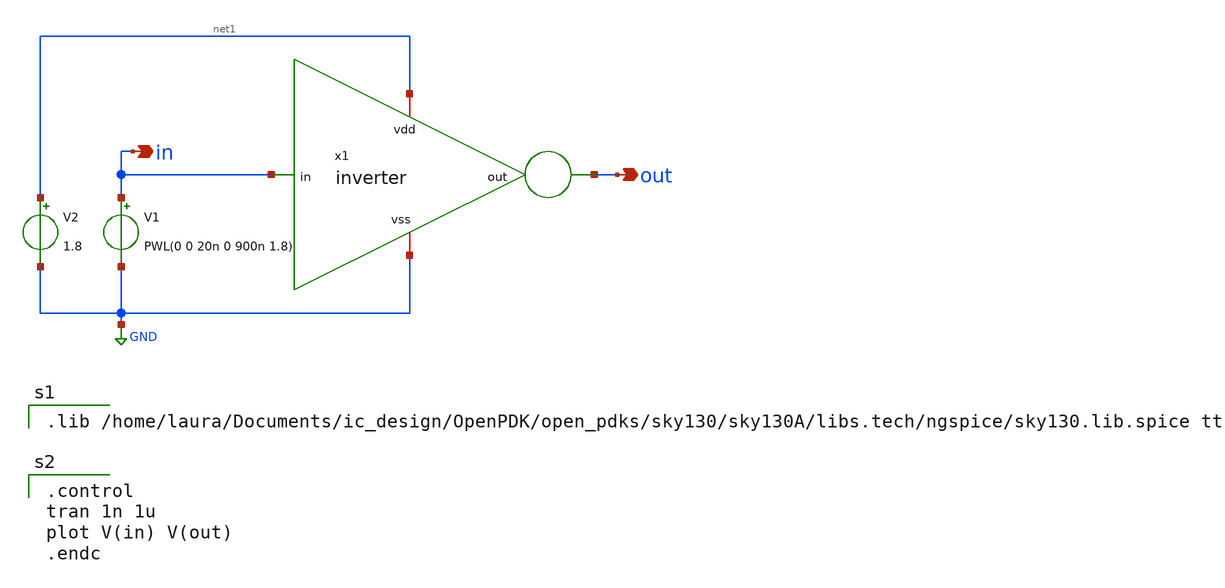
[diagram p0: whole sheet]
** sch_path: Inverter/xschem/inverter_tb.sch
**.subckt inverter_tb out in
*.opin out
*.opin in
x1 net1 in out GND inverter
V1 in GND PWL(0 0 20n 0 900n 1.8)
V2 net1 GND 1.8
**** begin user architecture code

.lib /home/laura/Documents/ic_design/OpenPDK/open_pdks/sky130/sky130A/libs.tech/ngspice/sky130.lib.spice tt


.control
tran 1n 1u
plot V(in) V(out)
.endc

**** end user architecture code
**.ends

* expanding   symbol:  inverter.sym # of pins=4
** sym_path: Inverter/xschem/inverter.sym
** sch_path: Inverter/xschem/inverter.sch
.subckt inverter vdd in out vss
*.ipin in
*.iopin vss
*.iopin vdd
*.opin out
XM1 out in vss vss sky130_fd_pr__nfet_01v8 L=0.18 W=1 nf=1 ad='int((nf+1)/2) * W/nf * 0.29' as='int((nf+2)/2) * W/nf * 0.29'
+ pd='2*int((nf+1)/2) * (W/nf + 0.29)' ps='2*int((nf+2)/2) * (W/nf + 0.29)' nrd='0.29 / W' nrs='0.29 / W'
+ sa=0 sb=0 sd=0 mult=1 m=1
XM2 out in vdd vdd sky130_fd_pr__pfet_01v8 L=0.18 W=3 nf=1 ad='int((nf+1)/2) * W/nf * 0.29' as='int((nf+2)/2) * W/nf * 0.29'
+ pd='2*int((nf+1)/2) * (W/nf + 0.29)' ps='2*int((nf+2)/2) * (W/nf + 0.29)' nrd='0.29 / W' nrs='0.29 / W'
+ sa=0 sb=0 sd=0 mult=1 m=1
.ends

.GLOBAL GND
.end
